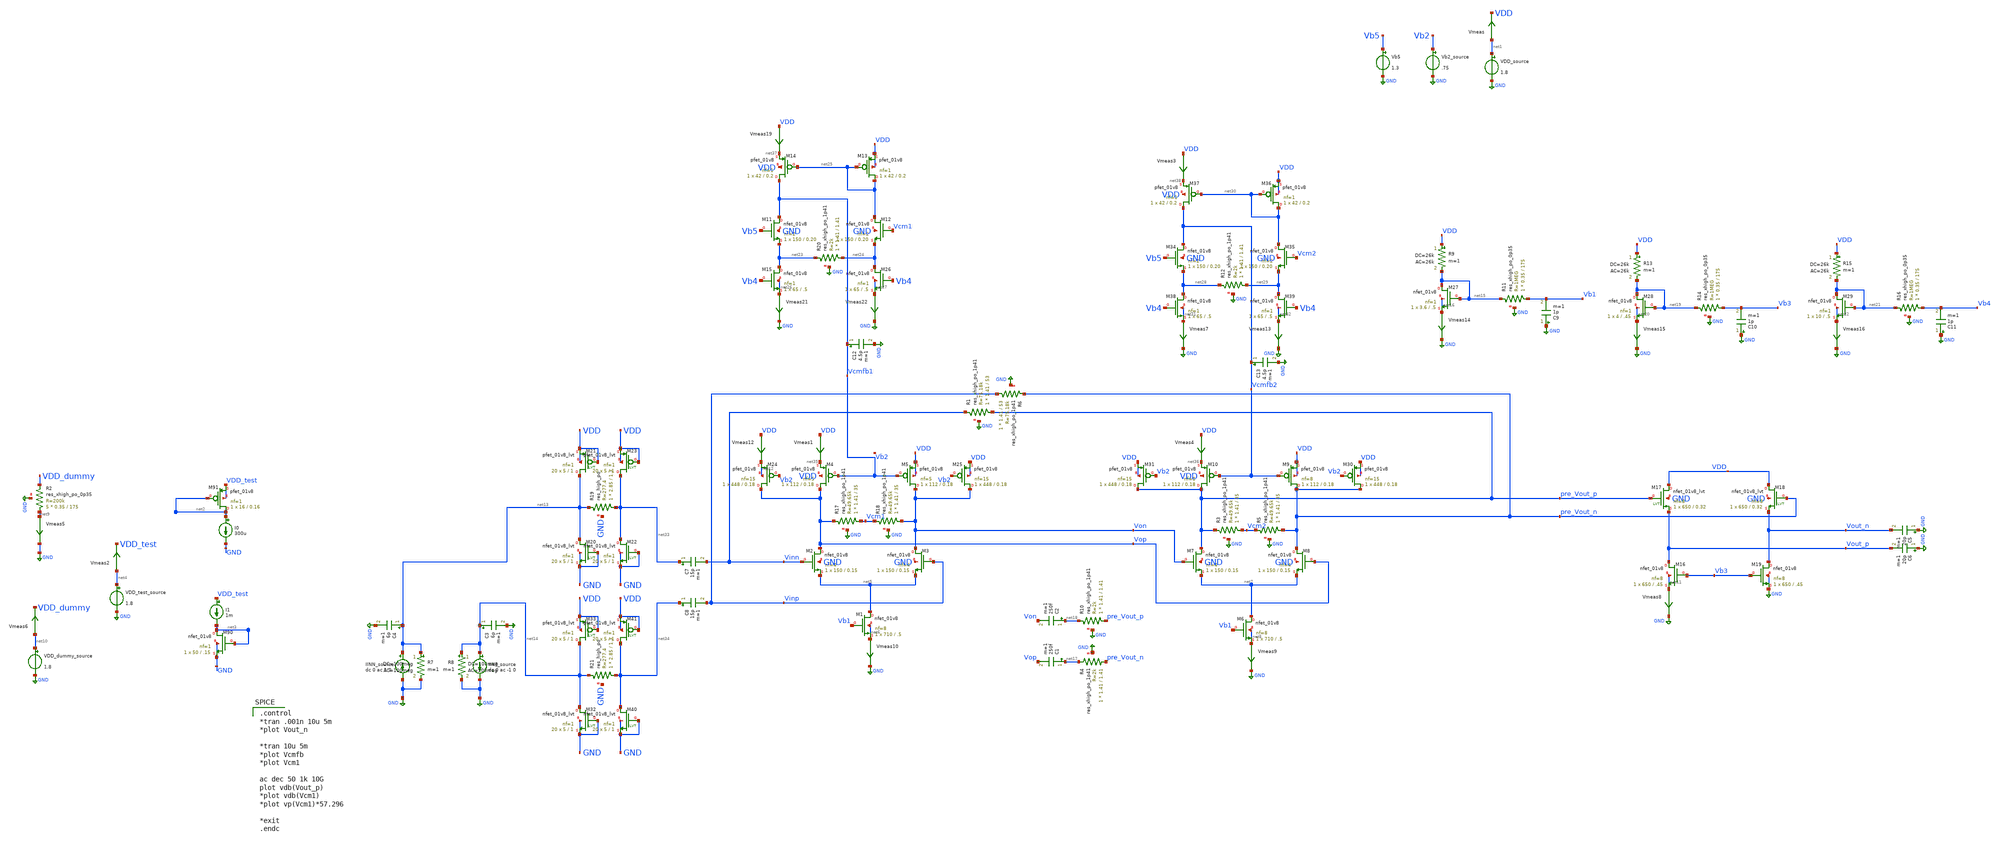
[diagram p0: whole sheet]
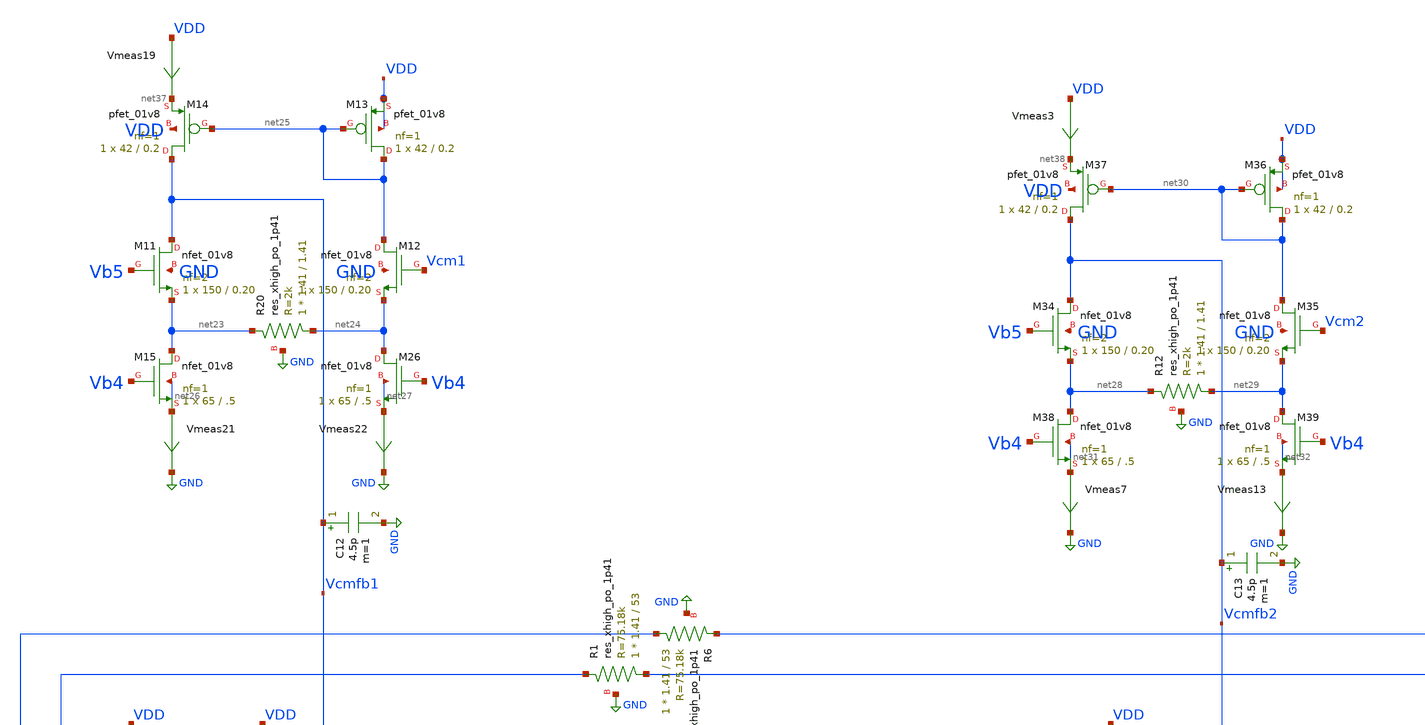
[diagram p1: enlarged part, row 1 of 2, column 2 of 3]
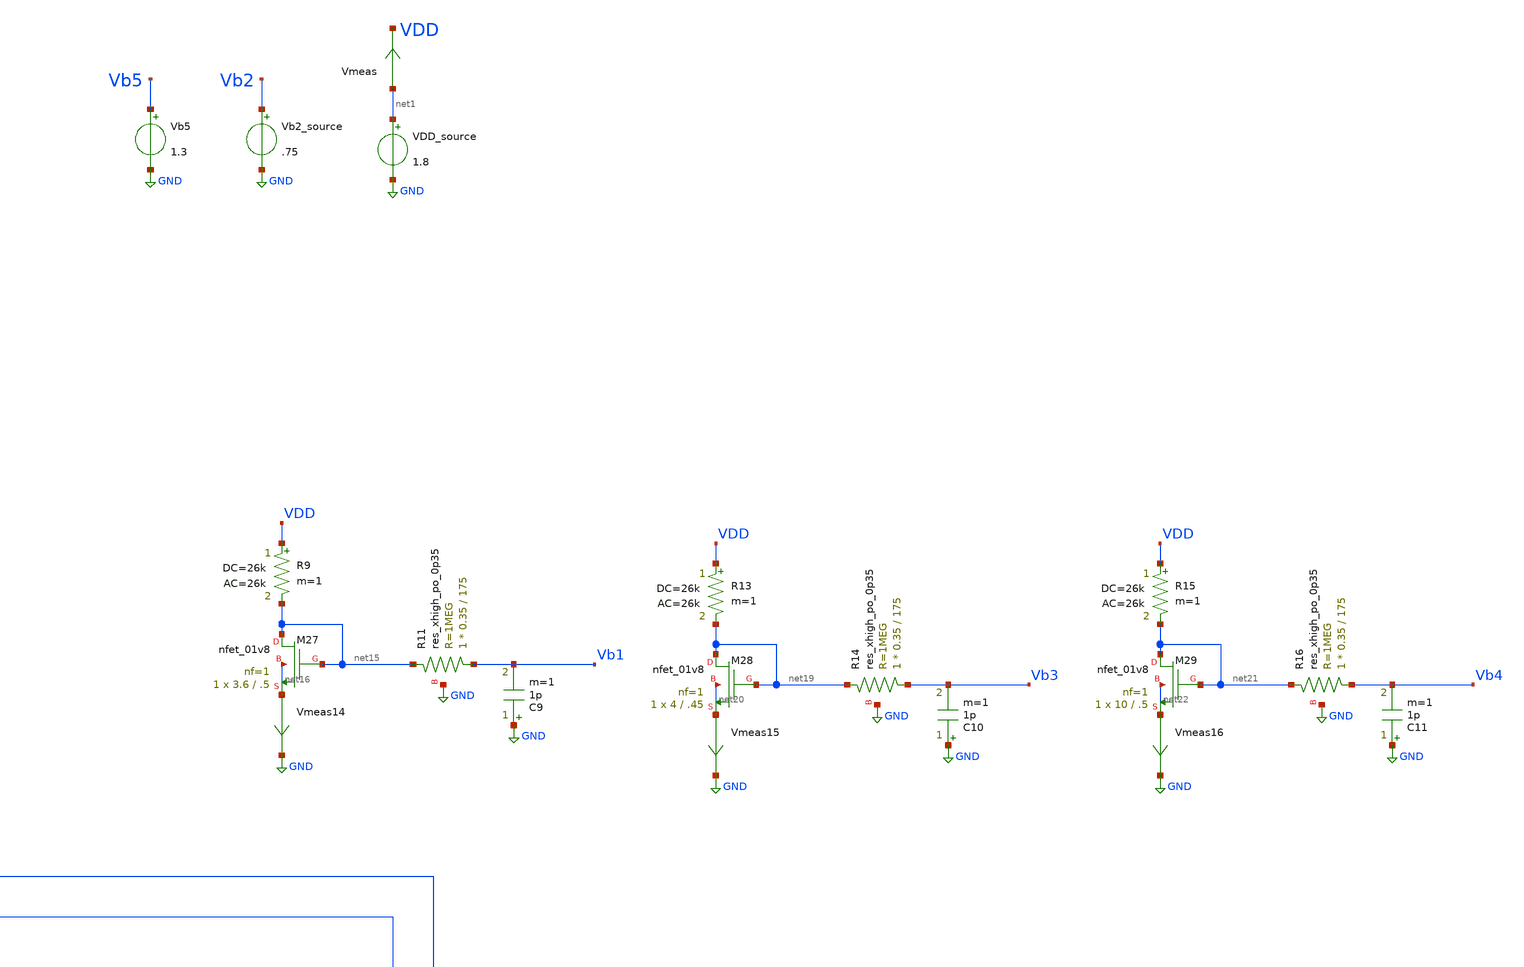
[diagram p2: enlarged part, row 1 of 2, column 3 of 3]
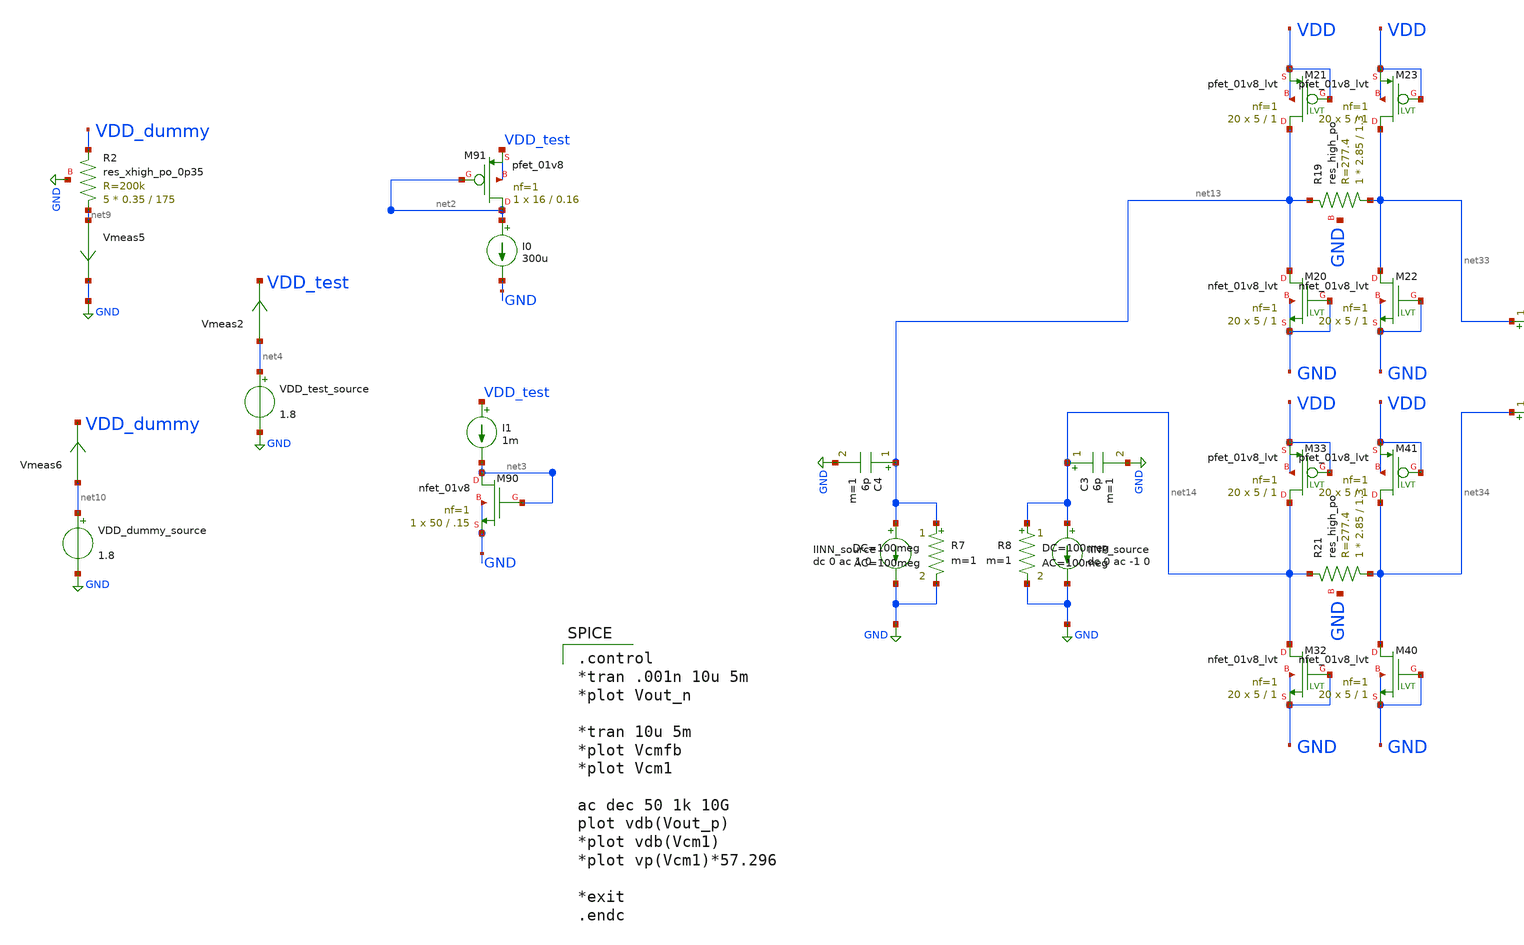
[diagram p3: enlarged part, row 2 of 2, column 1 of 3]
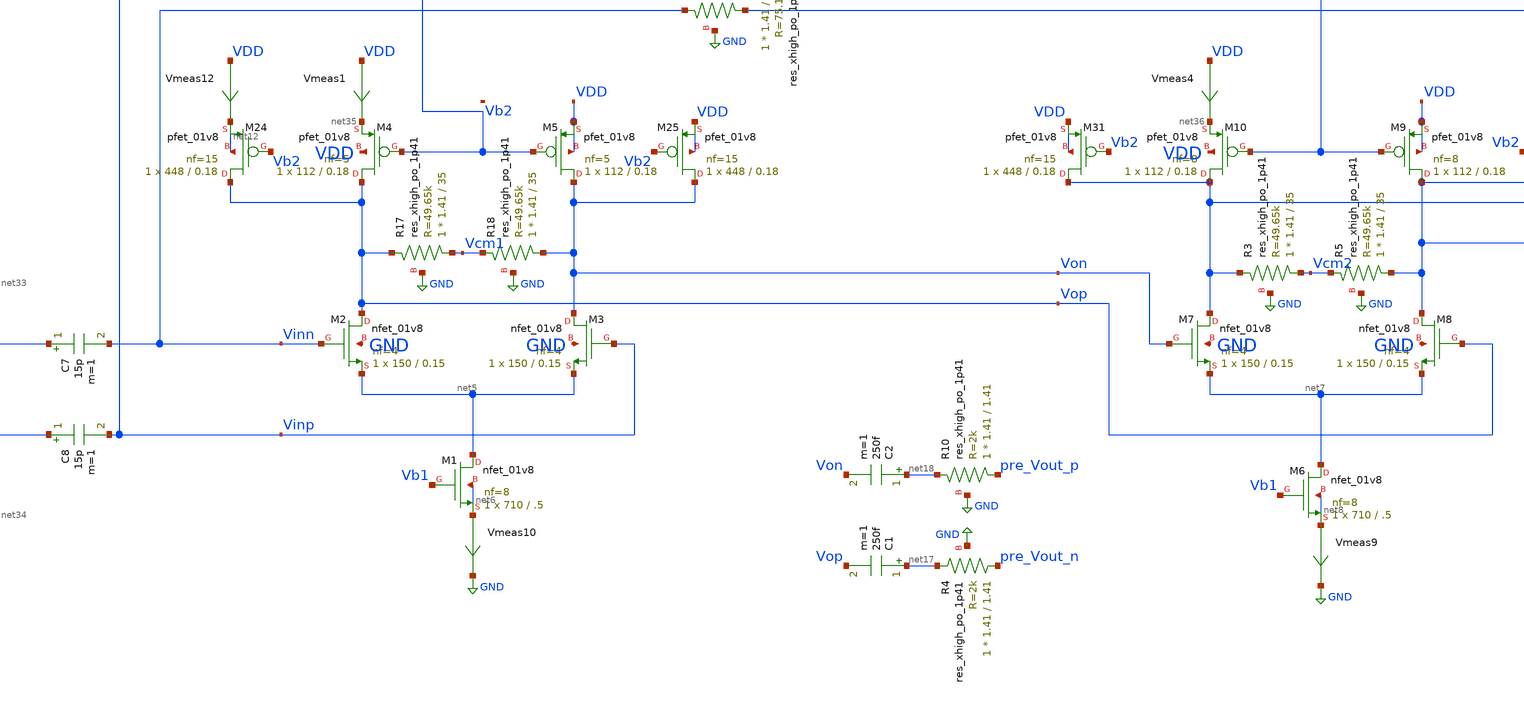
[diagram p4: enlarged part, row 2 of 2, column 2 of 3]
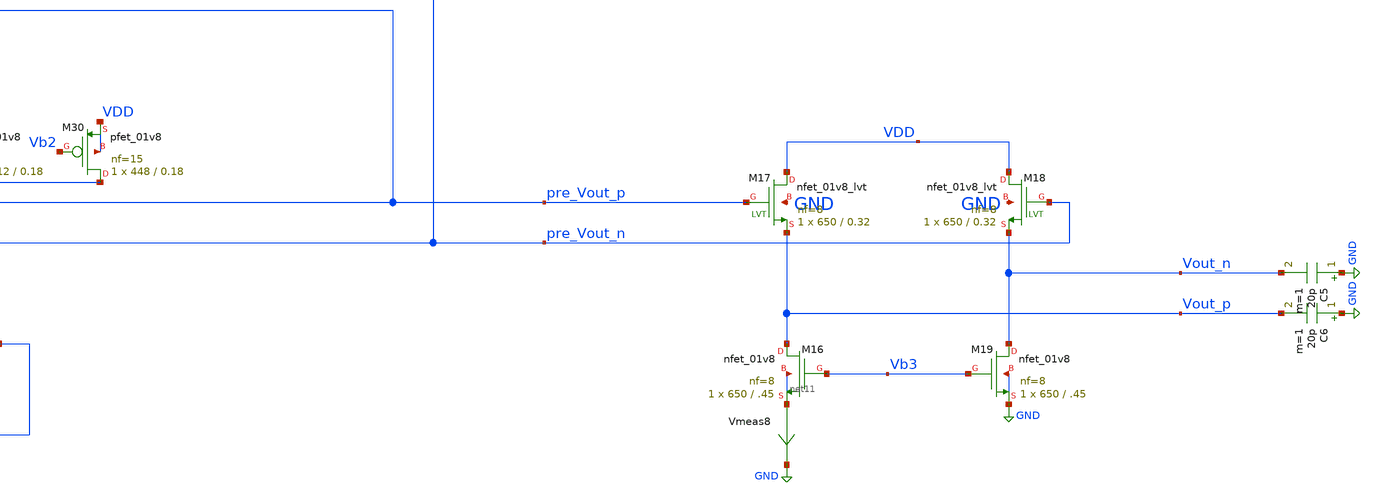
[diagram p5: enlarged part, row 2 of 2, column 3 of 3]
** sch_path: xschem/flattened_full_esd.sch
**.subckt flattened_full_esd
VDD_source net1 GND 1.8
Vmeas net1 VDD 0
.save i(vmeas)
XM90 net3 net3 GND GND sky130_fd_pr__nfet_01v8 L=.15 W=50 nf=1 ad='int((nf+1)/2) * W/nf * 0.29' as='int((nf+2)/2) * W/nf * 0.29'
+ pd='2*int((nf+1)/2) * (W/nf + 0.29)' ps='2*int((nf+2)/2) * (W/nf + 0.29)' nrd='0.29 / W' nrs='0.29 / W'
+ sa=0 sb=0 sd=0 mult=1 m=1
XM91 net2 net2 VDD_test VDD_test sky130_fd_pr__pfet_01v8 L=0.16 W=16 nf=1 ad='int((nf+1)/2) * W/nf * 0.29'
+ as='int((nf+2)/2) * W/nf * 0.29' pd='2*int((nf+1)/2) * (W/nf + 0.29)' ps='2*int((nf+2)/2) * (W/nf + 0.29)'
+ nrd='0.29 / W' nrs='0.29 / W' sa=0 sb=0 sd=0 mult=1 m=1
I0 net2 GND 300u
I1 VDD_test net3 1m
XM1 net5 Vb1 net6 net6 sky130_fd_pr__nfet_01v8 L=.5 W=710 nf=8 ad='int((nf+1)/2) * W/nf * 0.29' as='int((nf+2)/2) * W/nf * 0.29'
+ pd='2*int((nf+1)/2) * (W/nf + 0.29)' ps='2*int((nf+2)/2) * (W/nf + 0.29)' nrd='0.29 / W' nrs='0.29 / W'
+ sa=0 sb=0 sd=0 mult=1 m=1
VDD_test_source net4 GND 1.8
Vmeas2 net4 VDD_test 0
.save i(vmeas2)
XM2 Vop Vinn net5 GND sky130_fd_pr__nfet_01v8 L=0.15 W=150 nf=4 ad='int((nf+1)/2) * W/nf * 0.29' as='int((nf+2)/2) * W/nf * 0.29'
+ pd='2*int((nf+1)/2) * (W/nf + 0.29)' ps='2*int((nf+2)/2) * (W/nf + 0.29)' nrd='0.29 / W' nrs='0.29 / W'
+ sa=0 sb=0 sd=0 mult=1 m=1
XM3 Von Vinp net5 GND sky130_fd_pr__nfet_01v8 L=0.15 W=150 nf=4 ad='int((nf+1)/2) * W/nf * 0.29' as='int((nf+2)/2) * W/nf * 0.29'
+ pd='2*int((nf+1)/2) * (W/nf + 0.29)' ps='2*int((nf+2)/2) * (W/nf + 0.29)' nrd='0.29 / W' nrs='0.29 / W'
+ sa=0 sb=0 sd=0 mult=1 m=1
XM5 Von Vcmfb1 VDD VDD sky130_fd_pr__pfet_01v8 L=0.18 W=112 nf=5 ad='int((nf+1)/2) * W/nf * 0.29' as='int((nf+2)/2) * W/nf * 0.29'
+ pd='2*int((nf+1)/2) * (W/nf + 0.29)' ps='2*int((nf+2)/2) * (W/nf + 0.29)' nrd='0.29 / W' nrs='0.29 / W'
+ sa=0 sb=0 sd=0 mult=1 m=1
XM4 Vop Vcmfb1 net35 VDD sky130_fd_pr__pfet_01v8 L=0.18 W=112 nf=5 ad='int((nf+1)/2) * W/nf * 0.29' as='int((nf+2)/2) * W/nf * 0.29'
+ pd='2*int((nf+1)/2) * (W/nf + 0.29)' ps='2*int((nf+2)/2) * (W/nf + 0.29)' nrd='0.29 / W' nrs='0.29 / W'
+ sa=0 sb=0 sd=0 mult=1 m=1
Vb2_source Vb2 GND .75
Vmeas1 VDD net35 0
.save i(vmeas1)
XM6 net7 Vb1 net8 net8 sky130_fd_pr__nfet_01v8 L=.5 W=710 nf=8 ad='int((nf+1)/2) * W/nf * 0.29' as='int((nf+2)/2) * W/nf * 0.29'
+ pd='2*int((nf+1)/2) * (W/nf + 0.29)' ps='2*int((nf+2)/2) * (W/nf + 0.29)' nrd='0.29 / W' nrs='0.29 / W'
+ sa=0 sb=0 sd=0 mult=1 m=1
XM7 pre_Vout_p Von net7 GND sky130_fd_pr__nfet_01v8 L=0.15 W=150 nf=4 ad='int((nf+1)/2) * W/nf * 0.29'
+ as='int((nf+2)/2) * W/nf * 0.29' pd='2*int((nf+1)/2) * (W/nf + 0.29)' ps='2*int((nf+2)/2) * (W/nf + 0.29)'
+ nrd='0.29 / W' nrs='0.29 / W' sa=0 sb=0 sd=0 mult=1 m=1
XM8 pre_Vout_n Vop net7 GND sky130_fd_pr__nfet_01v8 L=0.15 W=150 nf=4 ad='int((nf+1)/2) * W/nf * 0.29'
+ as='int((nf+2)/2) * W/nf * 0.29' pd='2*int((nf+1)/2) * (W/nf + 0.29)' ps='2*int((nf+2)/2) * (W/nf + 0.29)'
+ nrd='0.29 / W' nrs='0.29 / W' sa=0 sb=0 sd=0 mult=1 m=1
XM9 pre_Vout_n Vcmfb2 VDD VDD sky130_fd_pr__pfet_01v8 L=0.18 W=112 nf=8 ad='int((nf+1)/2) * W/nf * 0.29'
+ as='int((nf+2)/2) * W/nf * 0.29' pd='2*int((nf+1)/2) * (W/nf + 0.29)' ps='2*int((nf+2)/2) * (W/nf + 0.29)'
+ nrd='0.29 / W' nrs='0.29 / W' sa=0 sb=0 sd=0 mult=1 m=1
XM10 pre_Vout_p Vcmfb2 net36 VDD sky130_fd_pr__pfet_01v8 L=0.18 W=112 nf=8 ad='int((nf+1)/2) * W/nf * 0.29'
+ as='int((nf+2)/2) * W/nf * 0.29' pd='2*int((nf+1)/2) * (W/nf + 0.29)' ps='2*int((nf+2)/2) * (W/nf + 0.29)'
+ nrd='0.29 / W' nrs='0.29 / W' sa=0 sb=0 sd=0 mult=1 m=1
Vmeas4 VDD net36 0
.save i(vmeas4)
Vmeas5 net9 GND 0
.save i(vmeas5)
C3 net14 GND 6p m=1
C4 net13 GND 6p m=1
VDD_dummy_source net10 GND 1.8
Vmeas6 net10 VDD_dummy 0
.save i(vmeas6)
IINN_source net13 GND dc 0 ac 1 0
IINP_source net14 GND dc 0 ac -1 0
XR6 Vinp pre_Vout_n GND sky130_fd_pr__res_xhigh_po_1p41 L=53 mult=1 m=1
XR1 pre_Vout_p Vinn GND sky130_fd_pr__res_xhigh_po_1p41 L=53 mult=1 m=1
XM16 Vout_p Vb3 net11 net11 sky130_fd_pr__nfet_01v8 L=.45 W=650 nf=8 ad='int((nf+1)/2) * W/nf * 0.29'
+ as='int((nf+2)/2) * W/nf * 0.29' pd='2*int((nf+1)/2) * (W/nf + 0.29)' ps='2*int((nf+2)/2) * (W/nf + 0.29)'
+ nrd='0.29 / W' nrs='0.29 / W' sa=0 sb=0 sd=0 mult=1 m=1
XM19 Vout_n Vb3 GND GND sky130_fd_pr__nfet_01v8 L=.45 W=650 nf=8 ad='int((nf+1)/2) * W/nf * 0.29' as='int((nf+2)/2) * W/nf * 0.29'
+ pd='2*int((nf+1)/2) * (W/nf + 0.29)' ps='2*int((nf+2)/2) * (W/nf + 0.29)' nrd='0.29 / W' nrs='0.29 / W'
+ sa=0 sb=0 sd=0 mult=1 m=1
Vmeas8 net11 GND 0
.save i(vmeas8)
XM17 VDD pre_Vout_p Vout_p GND sky130_fd_pr__nfet_01v8_lvt L=0.32 W=650 nf=8 ad='int((nf+1)/2) * W/nf * 0.29'
+ as='int((nf+2)/2) * W/nf * 0.29' pd='2*int((nf+1)/2) * (W/nf + 0.29)' ps='2*int((nf+2)/2) * (W/nf + 0.29)'
+ nrd='0.29 / W' nrs='0.29 / W' sa=0 sb=0 sd=0 mult=1 m=1
XM18 VDD pre_Vout_n Vout_n GND sky130_fd_pr__nfet_01v8_lvt L=0.32 W=650 nf=8 ad='int((nf+1)/2) * W/nf * 0.29'
+ as='int((nf+2)/2) * W/nf * 0.29' pd='2*int((nf+1)/2) * (W/nf + 0.29)' ps='2*int((nf+2)/2) * (W/nf + 0.29)'
+ nrd='0.29 / W' nrs='0.29 / W' sa=0 sb=0 sd=0 mult=1 m=1
C5 GND Vout_n 20p m=1
C6 GND Vout_p 20p m=1
Vmeas9 net8 GND 0
.save i(vmeas9)
Vmeas10 net6 GND 0
.save i(vmeas10)
XM24 Vop Vb2 net12 net12 sky130_fd_pr__pfet_01v8 L=0.18 W=448 nf=15 ad='int((nf+1)/2) * W/nf * 0.29'
+ as='int((nf+2)/2) * W/nf * 0.29' pd='2*int((nf+1)/2) * (W/nf + 0.29)' ps='2*int((nf+2)/2) * (W/nf + 0.29)'
+ nrd='0.29 / W' nrs='0.29 / W' sa=0 sb=0 sd=0 mult=1 m=1
XM25 Von Vb2 VDD VDD sky130_fd_pr__pfet_01v8 L=0.18 W=448 nf=15 ad='int((nf+1)/2) * W/nf * 0.29' as='int((nf+2)/2) * W/nf * 0.29'
+ pd='2*int((nf+1)/2) * (W/nf + 0.29)' ps='2*int((nf+2)/2) * (W/nf + 0.29)' nrd='0.29 / W' nrs='0.29 / W'
+ sa=0 sb=0 sd=0 mult=1 m=1
Vmeas12 VDD net12 0
.save i(vmeas12)
XM27 net15 net15 net16 net16 sky130_fd_pr__nfet_01v8 L=.5 W=3.6 nf=1 ad='int((nf+1)/2) * W/nf * 0.29'
+ as='int((nf+2)/2) * W/nf * 0.29' pd='2*int((nf+1)/2) * (W/nf + 0.29)' ps='2*int((nf+2)/2) * (W/nf + 0.29)'
+ nrd='0.29 / W' nrs='0.29 / W' sa=0 sb=0 sd=0 mult=1 m=1
Vmeas14 net16 GND 0
.save i(vmeas14)
R9 VDD net15 26k ac=26k m=1
R7 net13 GND 100meg ac=100meg m=1
R8 net14 GND 100meg ac=100meg m=1
C2 net18 Von 250f m=1
C1 net17 Vop 250f m=1
XR3 Vcm2 pre_Vout_p GND sky130_fd_pr__res_xhigh_po_1p41 L=35 mult=1 m=1
XR5 pre_Vout_n Vcm2 GND sky130_fd_pr__res_xhigh_po_1p41 L=35 mult=1 m=1
XR4 pre_Vout_n net17 GND sky130_fd_pr__res_xhigh_po_1p41 L=1.41 mult=1 m=1
XR10 pre_Vout_p net18 GND sky130_fd_pr__res_xhigh_po_1p41 L=1.41 mult=1 m=1
XR2 net9 VDD_dummy GND sky130_fd_pr__res_xhigh_po_0p35 L=175 mult=5 m=5
XR11 Vb1 net15 GND sky130_fd_pr__res_xhigh_po_0p35 L=175 mult=1 m=1
C9 GND Vb1 1p m=1
XM28 net19 net19 net20 net20 sky130_fd_pr__nfet_01v8 L=.45 W=4 nf=1 ad='int((nf+1)/2) * W/nf * 0.29'
+ as='int((nf+2)/2) * W/nf * 0.29' pd='2*int((nf+1)/2) * (W/nf + 0.29)' ps='2*int((nf+2)/2) * (W/nf + 0.29)'
+ nrd='0.29 / W' nrs='0.29 / W' sa=0 sb=0 sd=0 mult=1 m=1
Vmeas15 net20 GND 0
.save i(vmeas15)
R13 VDD net19 26k ac=26k m=1
XR14 Vb3 net19 GND sky130_fd_pr__res_xhigh_po_0p35 L=175 mult=1 m=1
C10 GND Vb3 1p m=1
XM29 net21 net21 net22 net22 sky130_fd_pr__nfet_01v8 L=.5 W=10 nf=1 ad='int((nf+1)/2) * W/nf * 0.29'
+ as='int((nf+2)/2) * W/nf * 0.29' pd='2*int((nf+1)/2) * (W/nf + 0.29)' ps='2*int((nf+2)/2) * (W/nf + 0.29)'
+ nrd='0.29 / W' nrs='0.29 / W' sa=0 sb=0 sd=0 mult=1 m=1
Vmeas16 net22 GND 0
.save i(vmeas16)
R15 VDD net21 26k ac=26k m=1
XR16 Vb4 net21 GND sky130_fd_pr__res_xhigh_po_0p35 L=175 mult=1 m=1
C11 GND Vb4 1p m=1
XR17 Vcm1 Vop GND sky130_fd_pr__res_xhigh_po_1p41 L=35 mult=1 m=1
XR18 Von Vcm1 GND sky130_fd_pr__res_xhigh_po_1p41 L=35 mult=1 m=1
XM30 pre_Vout_n Vb2 VDD VDD sky130_fd_pr__pfet_01v8 L=0.18 W=448 nf=15 ad='int((nf+1)/2) * W/nf * 0.29'
+ as='int((nf+2)/2) * W/nf * 0.29' pd='2*int((nf+1)/2) * (W/nf + 0.29)' ps='2*int((nf+2)/2) * (W/nf + 0.29)'
+ nrd='0.29 / W' nrs='0.29 / W' sa=0 sb=0 sd=0 mult=1 m=1
XM31 pre_Vout_p Vb2 VDD VDD sky130_fd_pr__pfet_01v8 L=0.18 W=448 nf=15 ad='int((nf+1)/2) * W/nf * 0.29'
+ as='int((nf+2)/2) * W/nf * 0.29' pd='2*int((nf+1)/2) * (W/nf + 0.29)' ps='2*int((nf+2)/2) * (W/nf + 0.29)'
+ nrd='0.29 / W' nrs='0.29 / W' sa=0 sb=0 sd=0 mult=1 m=1
XM11 Vcmfb1 Vb5 net23 GND sky130_fd_pr__nfet_01v8 L=0.20 W=150 nf=2 ad='int((nf+1)/2) * W/nf * 0.29'
+ as='int((nf+2)/2) * W/nf * 0.29' pd='2*int((nf+1)/2) * (W/nf + 0.29)' ps='2*int((nf+2)/2) * (W/nf + 0.29)'
+ nrd='0.29 / W' nrs='0.29 / W' sa=0 sb=0 sd=0 mult=1 m=1
XM12 net25 Vcm1 net24 GND sky130_fd_pr__nfet_01v8 L=0.20 W=150 nf=2 ad='int((nf+1)/2) * W/nf * 0.29'
+ as='int((nf+2)/2) * W/nf * 0.29' pd='2*int((nf+1)/2) * (W/nf + 0.29)' ps='2*int((nf+2)/2) * (W/nf + 0.29)'
+ nrd='0.29 / W' nrs='0.29 / W' sa=0 sb=0 sd=0 mult=1 m=1
XM13 net25 net25 VDD VDD sky130_fd_pr__pfet_01v8 L=0.2 W=42 nf=1 ad='int((nf+1)/2) * W/nf * 0.29' as='int((nf+2)/2) * W/nf * 0.29'
+ pd='2*int((nf+1)/2) * (W/nf + 0.29)' ps='2*int((nf+2)/2) * (W/nf + 0.29)' nrd='0.29 / W' nrs='0.29 / W'
+ sa=0 sb=0 sd=0 mult=1 m=1
XM14 Vcmfb1 net25 net37 VDD sky130_fd_pr__pfet_01v8 L=0.2 W=42 nf=1 ad='int((nf+1)/2) * W/nf * 0.29'
+ as='int((nf+2)/2) * W/nf * 0.29' pd='2*int((nf+1)/2) * (W/nf + 0.29)' ps='2*int((nf+2)/2) * (W/nf + 0.29)'
+ nrd='0.29 / W' nrs='0.29 / W' sa=0 sb=0 sd=0 mult=1 m=1
Vmeas19 VDD net37 0
.save i(vmeas19)
XM15 net23 Vb4 net26 net26 sky130_fd_pr__nfet_01v8 L=.5 W=65 nf=1 ad='int((nf+1)/2) * W/nf * 0.29' as='int((nf+2)/2) * W/nf * 0.29'
+ pd='2*int((nf+1)/2) * (W/nf + 0.29)' ps='2*int((nf+2)/2) * (W/nf + 0.29)' nrd='0.29 / W' nrs='0.29 / W'
+ sa=0 sb=0 sd=0 mult=1 m=1
Vmeas21 net26 GND 0
.save i(vmeas21)
XM26 net24 Vb4 net27 net27 sky130_fd_pr__nfet_01v8 L=.5 W=65 nf=1 ad='int((nf+1)/2) * W/nf * 0.29' as='int((nf+2)/2) * W/nf * 0.29'
+ pd='2*int((nf+1)/2) * (W/nf + 0.29)' ps='2*int((nf+2)/2) * (W/nf + 0.29)' nrd='0.29 / W' nrs='0.29 / W'
+ sa=0 sb=0 sd=0 mult=1 m=1
Vmeas22 net27 GND 0
.save i(vmeas22)
XR20 net24 net23 GND sky130_fd_pr__res_xhigh_po_1p41 L=1.41 mult=1 m=1
C7 net33 Vinn 15p m=1
C8 net34 Vinp 15p m=1
XM34 Vcmfb2 Vb5 net28 GND sky130_fd_pr__nfet_01v8 L=0.20 W=150 nf=2 ad='int((nf+1)/2) * W/nf * 0.29'
+ as='int((nf+2)/2) * W/nf * 0.29' pd='2*int((nf+1)/2) * (W/nf + 0.29)' ps='2*int((nf+2)/2) * (W/nf + 0.29)'
+ nrd='0.29 / W' nrs='0.29 / W' sa=0 sb=0 sd=0 mult=1 m=1
XM35 net30 Vcm2 net29 GND sky130_fd_pr__nfet_01v8 L=0.20 W=150 nf=2 ad='int((nf+1)/2) * W/nf * 0.29'
+ as='int((nf+2)/2) * W/nf * 0.29' pd='2*int((nf+1)/2) * (W/nf + 0.29)' ps='2*int((nf+2)/2) * (W/nf + 0.29)'
+ nrd='0.29 / W' nrs='0.29 / W' sa=0 sb=0 sd=0 mult=1 m=1
XM36 net30 net30 VDD VDD sky130_fd_pr__pfet_01v8 L=0.2 W=42 nf=1 ad='int((nf+1)/2) * W/nf * 0.29' as='int((nf+2)/2) * W/nf * 0.29'
+ pd='2*int((nf+1)/2) * (W/nf + 0.29)' ps='2*int((nf+2)/2) * (W/nf + 0.29)' nrd='0.29 / W' nrs='0.29 / W'
+ sa=0 sb=0 sd=0 mult=1 m=1
XM37 Vcmfb2 net30 net38 VDD sky130_fd_pr__pfet_01v8 L=0.2 W=42 nf=1 ad='int((nf+1)/2) * W/nf * 0.29'
+ as='int((nf+2)/2) * W/nf * 0.29' pd='2*int((nf+1)/2) * (W/nf + 0.29)' ps='2*int((nf+2)/2) * (W/nf + 0.29)'
+ nrd='0.29 / W' nrs='0.29 / W' sa=0 sb=0 sd=0 mult=1 m=1
Vmeas3 VDD net38 0
.save i(vmeas3)
XM38 net28 Vb4 net31 net31 sky130_fd_pr__nfet_01v8 L=.5 W=65 nf=1 ad='int((nf+1)/2) * W/nf * 0.29' as='int((nf+2)/2) * W/nf * 0.29'
+ pd='2*int((nf+1)/2) * (W/nf + 0.29)' ps='2*int((nf+2)/2) * (W/nf + 0.29)' nrd='0.29 / W' nrs='0.29 / W'
+ sa=0 sb=0 sd=0 mult=1 m=1
Vmeas7 net31 GND 0
.save i(vmeas7)
XM39 net29 Vb4 net32 net32 sky130_fd_pr__nfet_01v8 L=.5 W=65 nf=1 ad='int((nf+1)/2) * W/nf * 0.29' as='int((nf+2)/2) * W/nf * 0.29'
+ pd='2*int((nf+1)/2) * (W/nf + 0.29)' ps='2*int((nf+2)/2) * (W/nf + 0.29)' nrd='0.29 / W' nrs='0.29 / W'
+ sa=0 sb=0 sd=0 mult=1 m=1
Vmeas13 net32 GND 0
.save i(vmeas13)
XR12 net29 net28 GND sky130_fd_pr__res_xhigh_po_1p41 L=1.41 mult=1 m=1
Vb5 Vb5 GND 1.3
C12 Vcmfb1 GND 4.5p m=1
C13 Vcmfb2 GND 4.5p m=1
XM20 net13 GND GND GND sky130_fd_pr__nfet_01v8_lvt L=1 W=5 nf=1 ad='int((nf+1)/2) * W/nf * 0.29' as='int((nf+2)/2) * W/nf * 0.29'
+ pd='2*int((nf+1)/2) * (W/nf + 0.29)' ps='2*int((nf+2)/2) * (W/nf + 0.29)' nrd='0.29 / W' nrs='0.29 / W'
+ sa=0 sb=0 sd=0 mult=20 m=20
XM21 net13 VDD VDD VDD sky130_fd_pr__pfet_01v8_lvt L=1 W=5 nf=1 ad='int((nf+1)/2) * W/nf * 0.29' as='int((nf+2)/2) * W/nf * 0.29'
+ pd='2*int((nf+1)/2) * (W/nf + 0.29)' ps='2*int((nf+2)/2) * (W/nf + 0.29)' nrd='0.29 / W' nrs='0.29 / W'
+ sa=0 sb=0 sd=0 mult=20 m=20
XM22 net33 GND GND GND sky130_fd_pr__nfet_01v8_lvt L=1 W=5 nf=1 ad='int((nf+1)/2) * W/nf * 0.29' as='int((nf+2)/2) * W/nf * 0.29'
+ pd='2*int((nf+1)/2) * (W/nf + 0.29)' ps='2*int((nf+2)/2) * (W/nf + 0.29)' nrd='0.29 / W' nrs='0.29 / W'
+ sa=0 sb=0 sd=0 mult=20 m=20
XM23 net33 VDD VDD VDD sky130_fd_pr__pfet_01v8_lvt L=1 W=5 nf=1 ad='int((nf+1)/2) * W/nf * 0.29' as='int((nf+2)/2) * W/nf * 0.29'
+ pd='2*int((nf+1)/2) * (W/nf + 0.29)' ps='2*int((nf+2)/2) * (W/nf + 0.29)' nrd='0.29 / W' nrs='0.29 / W'
+ sa=0 sb=0 sd=0 mult=20 m=20
XR19 net33 net13 GND sky130_fd_pr__res_high_po W=2.85 L=1.3 mult=1 m=1
XM32 net14 GND GND GND sky130_fd_pr__nfet_01v8_lvt L=1 W=5 nf=1 ad='int((nf+1)/2) * W/nf * 0.29' as='int((nf+2)/2) * W/nf * 0.29'
+ pd='2*int((nf+1)/2) * (W/nf + 0.29)' ps='2*int((nf+2)/2) * (W/nf + 0.29)' nrd='0.29 / W' nrs='0.29 / W'
+ sa=0 sb=0 sd=0 mult=20 m=20
XM33 net14 VDD VDD VDD sky130_fd_pr__pfet_01v8_lvt L=1 W=5 nf=1 ad='int((nf+1)/2) * W/nf * 0.29' as='int((nf+2)/2) * W/nf * 0.29'
+ pd='2*int((nf+1)/2) * (W/nf + 0.29)' ps='2*int((nf+2)/2) * (W/nf + 0.29)' nrd='0.29 / W' nrs='0.29 / W'
+ sa=0 sb=0 sd=0 mult=20 m=20
XM40 net34 GND GND GND sky130_fd_pr__nfet_01v8_lvt L=1 W=5 nf=1 ad='int((nf+1)/2) * W/nf * 0.29' as='int((nf+2)/2) * W/nf * 0.29'
+ pd='2*int((nf+1)/2) * (W/nf + 0.29)' ps='2*int((nf+2)/2) * (W/nf + 0.29)' nrd='0.29 / W' nrs='0.29 / W'
+ sa=0 sb=0 sd=0 mult=20 m=20
XM41 net34 VDD VDD VDD sky130_fd_pr__pfet_01v8_lvt L=1 W=5 nf=1 ad='int((nf+1)/2) * W/nf * 0.29' as='int((nf+2)/2) * W/nf * 0.29'
+ pd='2*int((nf+1)/2) * (W/nf + 0.29)' ps='2*int((nf+2)/2) * (W/nf + 0.29)' nrd='0.29 / W' nrs='0.29 / W'
+ sa=0 sb=0 sd=0 mult=20 m=20
XR21 net34 net14 GND sky130_fd_pr__res_high_po W=2.85 L=1.3 mult=1 m=1
**** begin user architecture code

.include $::SKYWATER_MODELS/cells/nfet_01v8/sky130_fd_pr__nfet_01v8__tt.corner.spice
.include $::SKYWATER_MODELS/cells/pfet_01v8/sky130_fd_pr__pfet_01v8__tt.corner.spice
.include $::SKYWATER_MODELS/cells/nfet_01v8_lvt/sky130_fd_pr__nfet_01v8_lvt__tt.corner.spice
.include $::SKYWATER_MODELS/cells/pfet_01v8_lvt/sky130_fd_pr__pfet_01v8_lvt__tt.corner.spice
*.include $::SKYWATER_MODELS/cells/nfet_03v3_nvt/sky130_fd_pr__nfet_03v3_nvt__tt.corner.spice
*.include $::SKYWATER_MODELS/cells/nfet_05v0_nvt/sky130_fd_pr__nfet_05v0_nvt__tt.corner.spice
*.include $::SKYWATER_MODELS/cells/esd_nfet_01v8/sky130_fd_pr__esd_nfet_01v8__tt.corner.spice
*.include $::SKYWATER_MODELS/cells/pfet_01v8_hvt/sky130_fd_pr__pfet_01v8_hvt__tt.corner.spice
*.include $::SKYWATER_MODELS/models/corners/tt/nonfet.spice
* Mismatch parameters
.include $::SKYWATER_MODELS/cells/nfet_01v8/sky130_fd_pr__nfet_01v8__mismatch.corner.spice
.include $::SKYWATER_MODELS/cells/pfet_01v8/sky130_fd_pr__pfet_01v8__mismatch.corner.spice
.include $::SKYWATER_MODELS/cells/nfet_01v8_lvt/sky130_fd_pr__nfet_01v8_lvt__mismatch.corner.spice
.include $::SKYWATER_MODELS/cells/pfet_01v8_lvt/sky130_fd_pr__pfet_01v8_lvt__mismatch.corner.spice
*.include $::SKYWATER_MODELS/cells/pfet_01v8_hvt/sky130_fd_pr__pfet_01v8_hvt__mismatch.corner.spice
*.include $::SKYWATER_MODELS/cells/nfet_g5v0d10v5/sky130_fd_pr__nfet_g5v0d10v5__mismatch.corner.spice
*.include $::SKYWATER_MODELS/cells/pfet_g5v0d10v5/sky130_fd_pr__pfet_g5v0d10v5__mismatch.corner.spice
*.include $::SKYWATER_MODELS/cells/nfet_05v0_nvt/sky130_fd_pr__nfet_05v0_nvt__mismatch.corner.spice
*.include $::SKYWATER_MODELS/cells/nfet_03v3_nvt/sky130_fd_pr__nfet_03v3_nvt__mismatch.corner.spice
* Resistor$::SKYWATER_MODELS/Capacitor
.include $::SKYWATER_MODELS/models/r+c/res_typical__cap_typical.spice
.include $::SKYWATER_MODELS/models/r+c/res_typical__cap_typical__lin.spice
* Special cells
*.include $::SKYWATER_MODELS/models/corners/tt/specialized_cells.spice
* All models
.include $::SKYWATER_MODELS/models/all.spice
* Corner
*.include $::SKYWATER_MODELS/models/corners/tt/rf.spice


.option savecurrents
.control
save all
*NFET

save @m.xm90.msky130_fd_pr__nfet_01v8[vds] @m.xm90.msky130_fd_pr__nfet_01v8[gm]
+ @m.xm90.msky130_fd_pr__nfet_01v8[vth] @m.xm90.msky130_fd_pr__nfet_01v8[vgs] @m.xm90.msky130_fd_pr__nfet_01v8[id]
+ @m.xm90.msky130_fd_pr__nfet_01v8[gds] @m.xm90.msky130_fd_pr__nfet_01v8[cgg] @m.xm90.msky130_fd_pr__nfet_01v8[cgs]
+ @m.xm90.msky130_fd_pr__nfet_01v8[cgd] @m.xm90.msky130_fd_pr__nfet_01v8[cgb] @m.xm90.msky130_fd_pr__nfet_01v8[cdg]
+ @m.xm90.msky130_fd_pr__nfet_01v8[cds] @m.xm90.msky130_fd_pr__nfet_01v8[cdd] @m.xm90.msky130_fd_pr__nfet_01v8[cdb]
+ @m.xm90.msky130_fd_pr__nfet_01v8[csg] @m.xm90.msky130_fd_pr__nfet_01v8[css] @m.xm90.msky130_fd_pr__nfet_01v8[csd]
+ @m.xm90.msky130_fd_pr__nfet_01v8[csb] @m.xm90.msky130_fd_pr__nfet_01v8[cbg] @m.xm90.msky130_fd_pr__nfet_01v8[cbs]
+ @m.xm90.msky130_fd_pr__nfet_01v8[cbd] @m.xm90.msky130_fd_pr__nfet_01v8[cbb]
save @m.xm1.msky130_fd_pr__nfet_01v8[vds] @m.xm1.msky130_fd_pr__nfet_01v8[gm]
+ @m.xm1.msky130_fd_pr__nfet_01v8[vth] @m.xm1.msky130_fd_pr__nfet_01v8[vgs] @m.xm1.msky130_fd_pr__nfet_01v8[id]
+ @m.xm1.msky130_fd_pr__nfet_01v8[gds] @m.xm1.msky130_fd_pr__nfet_01v8[cgg] @m.xm1.msky130_fd_pr__nfet_01v8[cgs]
+ @m.xm1.msky130_fd_pr__nfet_01v8[cgd] @m.xm1.msky130_fd_pr__nfet_01v8[cgb] @m.xm1.msky130_fd_pr__nfet_01v8[cdg]
+ @m.xm1.msky130_fd_pr__nfet_01v8[cds] @m.xm1.msky130_fd_pr__nfet_01v8[cdd] @m.xm1.msky130_fd_pr__nfet_01v8[cdb]
+ @m.xm1.msky130_fd_pr__nfet_01v8[csg] @m.xm1.msky130_fd_pr__nfet_01v8[css] @m.xm1.msky130_fd_pr__nfet_01v8[csd]
+ @m.xm1.msky130_fd_pr__nfet_01v8[csb] @m.xm1.msky130_fd_pr__nfet_01v8[cbg] @m.xm1.msky130_fd_pr__nfet_01v8[cbs]
+ @m.xm1.msky130_fd_pr__nfet_01v8[cbd] @m.xm1.msky130_fd_pr__nfet_01v8[cbb]
save @m.xm2.msky130_fd_pr__nfet_01v8[vds] @m.xm2.msky130_fd_pr__nfet_01v8[gm]
+ @m.xm2.msky130_fd_pr__nfet_01v8[vth] @m.xm2.msky130_fd_pr__nfet_01v8[vgs] @m.xm2.msky130_fd_pr__nfet_01v8[id]
+ @m.xm2.msky130_fd_pr__nfet_01v8[gds] @m.xm2.msky130_fd_pr__nfet_01v8[cgg] @m.xm2.msky130_fd_pr__nfet_01v8[cgs]
+ @m.xm2.msky130_fd_pr__nfet_01v8[cgd] @m.xm2.msky130_fd_pr__nfet_01v8[cgb] @m.xm2.msky130_fd_pr__nfet_01v8[cdg]
+ @m.xm2.msky130_fd_pr__nfet_01v8[cds] @m.xm2.msky130_fd_pr__nfet_01v8[cdd] @m.xm2.msky130_fd_pr__nfet_01v8[cdb]
+ @m.xm2.msky130_fd_pr__nfet_01v8[csg] @m.xm2.msky130_fd_pr__nfet_01v8[css] @m.xm2.msky130_fd_pr__nfet_01v8[csd]
+ @m.xm2.msky130_fd_pr__nfet_01v8[csb] @m.xm2.msky130_fd_pr__nfet_01v8[cbg] @m.xm2.msky130_fd_pr__nfet_01v8[cbs]
+ @m.xm2.msky130_fd_pr__nfet_01v8[cbd] @m.xm2.msky130_fd_pr__nfet_01v8[cbb]
save @m.xm3.msky130_fd_pr__nfet_01v8[vds] @m.xm3.msky130_fd_pr__nfet_01v8[gm]
+ @m.xm3.msky130_fd_pr__nfet_01v8[vth] @m.xm3.msky130_fd_pr__nfet_01v8[vgs] @m.xm3.msky130_fd_pr__nfet_01v8[id]
+ @m.xm3.msky130_fd_pr__nfet_01v8[gds] @m.xm3.msky130_fd_pr__nfet_01v8[cgg] @m.xm3.msky130_fd_pr__nfet_01v8[cgs]
+ @m.xm3.msky130_fd_pr__nfet_01v8[cgd] @m.xm3.msky130_fd_pr__nfet_01v8[cgb] @m.xm3.msky130_fd_pr__nfet_01v8[cdg]
+ @m.xm3.msky130_fd_pr__nfet_01v8[cds] @m.xm3.msky130_fd_pr__nfet_01v8[cdd] @m.xm3.msky130_fd_pr__nfet_01v8[cdb]
+ @m.xm3.msky130_fd_pr__nfet_01v8[csg] @m.xm3.msky130_fd_pr__nfet_01v8[css] @m.xm3.msky130_fd_pr__nfet_01v8[csd]
+ @m.xm3.msky130_fd_pr__nfet_01v8[csb] @m.xm3.msky130_fd_pr__nfet_01v8[cbg] @m.xm3.msky130_fd_pr__nfet_01v8[cbs]
+ @m.xm3.msky130_fd_pr__nfet_01v8[cbd] @m.xm3.msky130_fd_pr__nfet_01v8[cbb]
save @m.xm6.msky130_fd_pr__nfet_01v8[vds] @m.xm6.msky130_fd_pr__nfet_01v8[gm]
+ @m.xm6.msky130_fd_pr__nfet_01v8[vth] @m.xm6.msky130_fd_pr__nfet_01v8[vgs] @m.xm6.msky130_fd_pr__nfet_01v8[id]
+ @m.xm6.msky130_fd_pr__nfet_01v8[gds] @m.xm6.msky130_fd_pr__nfet_01v8[cgg] @m.xm6.msky130_fd_pr__nfet_01v8[cgs]
+ @m.xm6.msky130_fd_pr__nfet_01v8[cgd] @m.xm6.msky130_fd_pr__nfet_01v8[cgb] @m.xm6.msky130_fd_pr__nfet_01v8[cdg]
+ @m.xm6.msky130_fd_pr__nfet_01v8[cds] @m.xm6.msky130_fd_pr__nfet_01v8[cdd] @m.xm6.msky130_fd_pr__nfet_01v8[cdb]
+ @m.xm6.msky130_fd_pr__nfet_01v8[csg] @m.xm6.msky130_fd_pr__nfet_01v8[css] @m.xm6.msky130_fd_pr__nfet_01v8[csd]
+ @m.xm6.msky130_fd_pr__nfet_01v8[csb] @m.xm6.msky130_fd_pr__nfet_01v8[cbg] @m.xm6.msky130_fd_pr__nfet_01v8[cbs]
+ @m.xm6.msky130_fd_pr__nfet_01v8[cbd] @m.xm6.msky130_fd_pr__nfet_01v8[cbb]
save @m.xm7.msky130_fd_pr__nfet_01v8[vds] @m.xm7.msky130_fd_pr__nfet_01v8[gm]
+ @m.xm7.msky130_fd_pr__nfet_01v8[vth] @m.xm7.msky130_fd_pr__nfet_01v8[vgs] @m.xm7.msky130_fd_pr__nfet_01v8[id]
+ @m.xm7.msky130_fd_pr__nfet_01v8[gds] @m.xm7.msky130_fd_pr__nfet_01v8[cgg] @m.xm7.msky130_fd_pr__nfet_01v8[cgs]
+ @m.xm7.msky130_fd_pr__nfet_01v8[cgd] @m.xm7.msky130_fd_pr__nfet_01v8[cgb] @m.xm7.msky130_fd_pr__nfet_01v8[cdg]
+ @m.xm7.msky130_fd_pr__nfet_01v8[cds] @m.xm7.msky130_fd_pr__nfet_01v8[cdd] @m.xm7.msky130_fd_pr__nfet_01v8[cdb]
+ @m.xm7.msky130_fd_pr__nfet_01v8[csg] @m.xm7.msky130_fd_pr__nfet_01v8[css] @m.xm7.msky130_fd_pr__nfet_01v8[csd]
+ @m.xm7.msky130_fd_pr__nfet_01v8[csb] @m.xm7.msky130_fd_pr__nfet_01v8[cbg] @m.xm7.msky130_fd_pr__nfet_01v8[cbs]
+ @m.xm7.msky130_fd_pr__nfet_01v8[cbd] @m.xm7.msky130_fd_pr__nfet_01v8[cbb]
save @m.xm8.msky130_fd_pr__nfet_01v8[vds] @m.xm8.msky130_fd_pr__nfet_01v8[gm]
+ @m.xm8.msky130_fd_pr__nfet_01v8[vth] @m.xm8.msky130_fd_pr__nfet_01v8[vgs] @m.xm8.msky130_fd_pr__nfet_01v8[id]
+ @m.xm8.msky130_fd_pr__nfet_01v8[gds] @m.xm8.msky130_fd_pr__nfet_01v8[cgg] @m.xm8.msky130_fd_pr__nfet_01v8[cgs]
+ @m.xm8.msky130_fd_pr__nfet_01v8[cgd] @m.xm8.msky130_fd_pr__nfet_01v8[cgb] @m.xm8.msky130_fd_pr__nfet_01v8[cdg]
+ @m.xm8.msky130_fd_pr__nfet_01v8[cds] @m.xm8.msky130_fd_pr__nfet_01v8[cdd] @m.xm8.msky130_fd_pr__nfet_01v8[cdb]
+ @m.xm8.msky130_fd_pr__nfet_01v8[csg] @m.xm8.msky130_fd_pr__nfet_01v8[css] @m.xm8.msky130_fd_pr__nfet_01v8[csd]
+ @m.xm8.msky130_fd_pr__nfet_01v8[csb] @m.xm8.msky130_fd_pr__nfet_01v8[cbg] @m.xm8.msky130_fd_pr__nfet_01v8[cbs]
+ @m.xm8.msky130_fd_pr__nfet_01v8[cbd] @m.xm8.msky130_fd_pr__nfet_01v8[cbb]
save @m.xm11.msky130_fd_pr__nfet_01v8[vds] @m.xm11.msky130_fd_pr__nfet_01v8[gm]
+ @m.xm11.msky130_fd_pr__nfet_01v8[vth] @m.xm11.msky130_fd_pr__nfet_01v8[vgs] @m.xm11.msky130_fd_pr__nfet_01v8[id]
+ @m.xm11.msky130_fd_pr__nfet_01v8[gds] @m.xm11.msky130_fd_pr__nfet_01v8[cgg] @m.xm11.msky130_fd_pr__nfet_01v8[cgs]
+ @m.xm11.msky130_fd_pr__nfet_01v8[cgd] @m.xm11.msky130_fd_pr__nfet_01v8[cgb] @m.xm11.msky130_fd_pr__nfet_01v8[cdg]
+ @m.xm11.msky130_fd_pr__nfet_01v8[cds] @m.xm11.msky130_fd_pr__nfet_01v8[cdd] @m.xm11.msky130_fd_pr__nfet_01v8[cdb]
+ @m.xm11.msky130_fd_pr__nfet_01v8[csg] @m.xm11.msky130_fd_pr__nfet_01v8[css] @m.xm11.msky130_fd_pr__nfet_01v8[csd]
+ @m.xm11.msky130_fd_pr__nfet_01v8[csb] @m.xm11.msky130_fd_pr__nfet_01v8[cbg] @m.xm11.msky130_fd_pr__nfet_01v8[cbs]
+ @m.xm11.msky130_fd_pr__nfet_01v8[cbd] @m.xm11.msky130_fd_pr__nfet_01v8[cbb]
save @m.xm12.msky130_fd_pr__nfet_01v8[vds] @m.xm12.msky130_fd_pr__nfet_01v8[gm]
+ @m.xm12.msky130_fd_pr__nfet_01v8[vth] @m.xm12.msky130_fd_pr__nfet_01v8[vgs] @m.xm12.msky130_fd_pr__nfet_01v8[id]
+ @m.xm12.msky130_fd_pr__nfet_01v8[gds] @m.xm12.msky130_fd_pr__nfet_01v8[cgg] @m.xm12.msky130_fd_pr__nfet_01v8[cgs]
+ @m.xm12.msky130_fd_pr__nfet_01v8[cgd] @m.xm12.msky130_fd_pr__nfet_01v8[cgb] @m.xm12.msky130_fd_pr__nfet_01v8[cdg]
+ @m.xm12.msky130_fd_pr__nfet_01v8[cds] @m.xm12.msky130_fd_pr__nfet_01v8[cdd] @m.xm12.msky130_fd_pr__nfet_01v8[cdb]
+ @m.xm12.msky130_fd_pr__nfet_01v8[csg] @m.xm12.msky130_fd_pr__nfet_01v8[css] @m.xm12.msky130_fd_pr__nfet_01v8[csd]
+ @m.xm12.msky130_fd_pr__nfet_01v8[csb] @m.xm12.msky130_fd_pr__nfet_01v8[cbg] @m.xm12.msky130_fd_pr__nfet_01v8[cbs]
+ @m.xm12.msky130_fd_pr__nfet_01v8[cbd] @m.xm12.msky130_fd_pr__nfet_01v8[cbb]
save @m.xm16.msky130_fd_pr__nfet_01v8[vds] @m.xm16.msky130_fd_pr__nfet_01v8[gm]
+ @m.xm16.msky130_fd_pr__nfet_01v8[vth] @m.xm16.msky130_fd_pr__nfet_01v8[vgs] @m.xm16.msky130_fd_pr__nfet_01v8[id]
+ @m.xm16.msky130_fd_pr__nfet_01v8[gds] @m.xm16.msky130_fd_pr__nfet_01v8[cgg] @m.xm16.msky130_fd_pr__nfet_01v8[cgs]
+ @m.xm16.msky130_fd_pr__nfet_01v8[cgd] @m.xm16.msky130_fd_pr__nfet_01v8[cgb] @m.xm16.msky130_fd_pr__nfet_01v8[cdg]
+ @m.xm16.msky130_fd_pr__nfet_01v8[cds] @m.xm16.msky130_fd_pr__nfet_01v8[cdd] @m.xm16.msky130_fd_pr__nfet_01v8[cdb]
+ @m.xm16.msky130_fd_pr__nfet_01v8[csg] @m.xm16.msky130_fd_pr__nfet_01v8[css] @m.xm16.msky130_fd_pr__nfet_01v8[csd]
+ @m.xm16.msky130_fd_pr__nfet_01v8[csb] @m.xm16.msky130_fd_pr__nfet_01v8[cbg] @m.xm16.msky130_fd_pr__nfet_01v8[cbs]
+ @m.xm16.msky130_fd_pr__nfet_01v8[cbd] @m.xm16.msky130_fd_pr__nfet_01v8[cbb]
save @m.xm17.msky130_fd_pr__nfet_01v8_lvt[vds] @m.xm17.msky130_fd_pr__nfet_01v8_lvt[gm]
+ @m.xm17.msky130_fd_pr__nfet_01v8_lvt[vth] @m.xm17.msky130_fd_pr__nfet_01v8_lvt[vgs] @m.xm17.msky130_fd_pr__nfet_01v8_lvt[id]
+ @m.xm17.msky130_fd_pr__nfet_01v8_lvt[gds] @m.xm17.msky130_fd_pr__nfet_01v8_lvt[cgg] @m.xm17.msky130_fd_pr__nfet_01v8_lvt[cgs]
+ @m.xm17.msky130_fd_pr__nfet_01v8_lvt[cgd] @m.xm17.msky130_fd_pr__nfet_01v8_lvt[cgb] @m.xm17.msky130_fd_pr__nfet_01v8_lvt[cdg]
+ @m.xm17.msky130_fd_pr__nfet_01v8_lvt[cds] @m.xm17.msky130_fd_pr__nfet_01v8_lvt[cdd] @m.xm17.msky130_fd_pr__nfet_01v8_lvt[cdb]
+ @m.xm17.msky130_fd_pr__nfet_01v8_lvt[csg] @m.xm17.msky130_fd_pr__nfet_01v8_lvt[css] @m.xm17.msky130_fd_pr__nfet_01v8_lvt[csd]
+ @m.xm17.msky130_fd_pr__nfet_01v8_lvt[csb] @m.xm17.msky130_fd_pr__nfet_01v8_lvt[cbg] @m.xm17.msky130_fd_pr__nfet_01v8_lvt[cbs]
+ @m.xm17.msky130_fd_pr__nfet_01v8_lvt[cbd] @m.xm17.msky130_fd_pr__nfet_01v8_lvt[cbb]
save @m.xm18.msky130_fd_pr__nfet_01v8_lvt[vds] @m.xm18.msky130_fd_pr__nfet_01v8_lvt[gm]
+ @m.xm18.msky130_fd_pr__nfet_01v8_lvt[vth] @m.xm18.msky130_fd_pr__nfet_01v8_lvt[vgs] @m.xm18.msky130_fd_pr__nfet_01v8_lvt[id]
+ @m.xm18.msky130_fd_pr__nfet_01v8_lvt[gds] @m.xm18.msky130_fd_pr__nfet_01v8_lvt[cgg] @m.xm18.msky130_fd_pr__nfet_01v8_lvt[cgs]
+ @m.xm18.msky130_fd_pr__nfet_01v8_lvt[cgd] @m.xm18.msky130_fd_pr__nfet_01v8_lvt[cgb] @m.xm18.msky130_fd_pr__nfet_01v8_lvt[cdg]
+ @m.xm18.msky130_fd_pr__nfet_01v8_lvt[cds] @m.xm18.msky130_fd_pr__nfet_01v8_lvt[cdd] @m.xm18.msky130_fd_pr__nfet_01v8_lvt[cdb]
+ @m.xm18.msky130_fd_pr__nfet_01v8_lvt[csg] @m.xm18.msky130_fd_pr__nfet_01v8_lvt[css] @m.xm18.msky130_fd_pr__nfet_01v8_lvt[csd]
+ @m.xm18.msky130_fd_pr__nfet_01v8_lvt[csb] @m.xm18.msky130_fd_pr__nfet_01v8_lvt[cbg] @m.xm18.msky130_fd_pr__nfet_01v8_lvt[cbs]
+ @m.xm18.msky130_fd_pr__nfet_01v8_lvt[cbd] @m.xm18.msky130_fd_pr__nfet_01v8_lvt[cbb]
save @m.xm19.msky130_fd_pr__nfet_01v8[vds] @m.xm19.msky130_fd_pr__nfet_01v8[gm]
+ @m.xm19.msky130_fd_pr__nfet_01v8[vth] @m.xm19.msky130_fd_pr__nfet_01v8[vgs] @m.xm19.msky130_fd_pr__nfet_01v8[id]
+ @m.xm19.msky130_fd_pr__nfet_01v8[gds] @m.xm19.msky130_fd_pr__nfet_01v8[cgg] @m.xm19.msky130_fd_pr__nfet_01v8[cgs]
+ @m.xm19.msky130_fd_pr__nfet_01v8[cgd] @m.xm19.msky130_fd_pr__nfet_01v8[cgb] @m.xm19.msky130_fd_pr__nfet_01v8[cdg]
+ @m.xm19.msky130_fd_pr__nfet_01v8[cds] @m.xm19.msky130_fd_pr__nfet_01v8[cdd] @m.xm19.msky130_fd_pr__nfet_01v8[cdb]
+ @m.xm19.msky130_fd_pr__nfet_01v8[csg] @m.xm19.msky130_fd_pr__nfet_01v8[css] @m.xm19.msky130_fd_pr__nfet_01v8[csd]
+ @m.xm19.msky130_fd_pr__nfet_01v8[csb] @m.xm19.msky130_fd_pr__nfet_01v8[cbg] @m.xm19.msky130_fd_pr__nfet_01v8[cbs]
+ @m.xm19.msky130_fd_pr__nfet_01v8[cbd] @m.xm19.msky130_fd_pr__nfet_01v8[cbb]
save @m.xm30.msky130_fd_pr__nfet_01v8[vds] @m.xm30.msky130_fd_pr__nfet_01v8[gm]
+ @m.xm30.msky130_fd_pr__nfet_01v8[vth] @m.xm30.msky130_fd_pr__nfet_01v8[vgs] @m.xm30.msky130_fd_pr__nfet_01v8[id]
+ @m.xm30.msky130_fd_pr__nfet_01v8[gds] @m.xm30.msky130_fd_pr__nfet_01v8[cgg] @m.xm30.msky130_fd_pr__nfet_01v8[cgs]
+ @m.xm30.msky130_fd_pr__nfet_01v8[cgd] @m.xm30.msky130_fd_pr__nfet_01v8[cgb] @m.xm30.msky130_fd_pr__nfet_01v8[cdg]
+ @m.xm30.msky130_fd_pr__nfet_01v8[cds] @m.xm30.msky130_fd_pr__nfet_01v8[cdd] @m.xm30.msky130_fd_pr__nfet_01v8[cdb]
+ @m.xm30.msky130_fd_pr__nfet_01v8[csg] @m.xm30.msky130_fd_pr__nfet_01v8[css] @m.xm30.msky130_fd_pr__nfet_01v8[csd]
+ @m.xm30.msky130_fd_pr__nfet_01v8[csb] @m.xm30.msky130_fd_pr__nfet_01v8[cbg] @m.xm30.msky130_fd_pr__nfet_01v8[cbs]
+ @m.xm30.msky130_fd_pr__nfet_01v8[cbd] @m.xm30.msky130_fd_pr__nfet_01v8[cbb]
save @m.xm26.msky130_fd_pr__nfet_01v8[vds] @m.xm26.msky130_fd_pr__nfet_01v8[gm]
+ @m.xm26.msky130_fd_pr__nfet_01v8[vth] @m.xm26.msky130_fd_pr__nfet_01v8[vgs] @m.xm26.msky130_fd_pr__nfet_01v8[id]
+ @m.xm26.msky130_fd_pr__nfet_01v8[gds] @m.xm26.msky130_fd_pr__nfet_01v8[cgg] @m.xm26.msky130_fd_pr__nfet_01v8[cgs]
+ @m.xm26.msky130_fd_pr__nfet_01v8[cgd] @m.xm26.msky130_fd_pr__nfet_01v8[cgb] @m.xm26.msky130_fd_pr__nfet_01v8[cdg]
+ @m.xm26.msky130_fd_pr__nfet_01v8[cds] @m.xm26.msky130_fd_pr__nfet_01v8[cdd] @m.xm26.msky130_fd_pr__nfet_01v8[cdb]
+ @m.xm26.msky130_fd_pr__nfet_01v8[csg] @m.xm26.msky130_fd_pr__nfet_01v8[css] @m.xm26.msky130_fd_pr__nfet_01v8[csd]
+ @m.xm26.msky130_fd_pr__nfet_01v8[csb] @m.xm26.msky130_fd_pr__nfet_01v8[cbg] @m.xm26.msky130_fd_pr__nfet_01v8[cbs]
+ @m.xm26.msky130_fd_pr__nfet_01v8[cbd] @m.xm26.msky130_fd_pr__nfet_01v8[cbb]
save @m.xm27.msky130_fd_pr__nfet_01v8[vds] @m.xm27.msky130_fd_pr__nfet_01v8[gm]
+ @m.xm27.msky130_fd_pr__nfet_01v8[vth] @m.xm27.msky130_fd_pr__nfet_01v8[vgs] @m.xm27.msky130_fd_pr__nfet_01v8[id]
+ @m.xm27.msky130_fd_pr__nfet_01v8[gds] @m.xm27.msky130_fd_pr__nfet_01v8[cgg] @m.xm27.msky130_fd_pr__nfet_01v8[cgs]
+ @m.xm27.msky130_fd_pr__nfet_01v8[cgd] @m.xm27.msky130_fd_pr__nfet_01v8[cgb] @m.xm27.msky130_fd_pr__nfet_01v8[cdg]
+ @m.xm27.msky130_fd_pr__nfet_01v8[cds] @m.xm27.msky130_fd_pr__nfet_01v8[cdd] @m.xm27.msky130_fd_pr__nfet_01v8[cdb]
+ @m.xm27.msky130_fd_pr__nfet_01v8[csg] @m.xm27.msky130_fd_pr__nfet_01v8[css] @m.xm27.msky130_fd_pr__nfet_01v8[csd]
+ @m.xm27.msky130_fd_pr__nfet_01v8[csb] @m.xm27.msky130_fd_pr__nfet_01v8[cbg] @m.xm27.msky130_fd_pr__nfet_01v8[cbs]
+ @m.xm27.msky130_fd_pr__nfet_01v8[cbd] @m.xm27.msky130_fd_pr__nfet_01v8[cbb]

*PFET

save @m.xm91.msky130_fd_pr__pfet_01v8[vds] @m.xm91.msky130_fd_pr__pfet_01v8[gm]
+ @m.xm91.msky130_fd_pr__pfet_01v8[vth] @m.xm91.msky130_fd_pr__pfet_01v8[vgs] @m.xm91.msky130_fd_pr__pfet_01v8[id]
+ @m.xm91.msky130_fd_pr__pfet_01v8[gds] @m.xm91.msky130_fd_pr__pfet_01v8[cgg] @m.xm91.msky130_fd_pr__pfet_01v8[cgs]
+ @m.xm91.msky130_fd_pr__pfet_01v8[cgd] @m.xm91.msky130_fd_pr__pfet_01v8[cgb] @m.xm91.msky130_fd_pr__pfet_01v8[cdg]
+ @m.xm91.msky130_fd_pr__pfet_01v8[cds] @m.xm91.msky130_fd_pr__pfet_01v8[cdd] @m.xm91.msky130_fd_pr__pfet_01v8[cdb]
+ @m.xm91.msky130_fd_pr__pfet_01v8[csg] @m.xm91.msky130_fd_pr__pfet_01v8[css] @m.xm91.msky130_fd_pr__pfet_01v8[csd]
+ @m.xm91.msky130_fd_pr__pfet_01v8[csb] @m.xm91.msky130_fd_pr__pfet_01v8[cbg] @m.xm91.msky130_fd_pr__pfet_01v8[cbs]
+ @m.xm91.msky130_fd_pr__pfet_01v8[cbd] @m.xm91.msky130_fd_pr__pfet_01v8[cbb]
save @m.xm4.msky130_fd_pr__pfet_01v8[vds] @m.xm4.msky130_fd_pr__pfet_01v8[gm]
+ @m.xm4.msky130_fd_pr__pfet_01v8[vth] @m.xm4.msky130_fd_pr__pfet_01v8[vgs] @m.xm4.msky130_fd_pr__pfet_01v8[id]
+ @m.xm4.msky130_fd_pr__pfet_01v8[gds] @m.xm4.msky130_fd_pr__pfet_01v8[cgg] @m.xm4.msky130_fd_pr__pfet_01v8[cgs]
+ @m.xm4.msky130_fd_pr__pfet_01v8[cgd] @m.xm4.msky130_fd_pr__pfet_01v8[cgb] @m.xm4.msky130_fd_pr__pfet_01v8[cdg]
+ @m.xm4.msky130_fd_pr__pfet_01v8[cds] @m.xm4.msky130_fd_pr__pfet_01v8[cdd] @m.xm4.msky130_fd_pr__pfet_01v8[cdb]
+ @m.xm4.msky130_fd_pr__pfet_01v8[csg] @m.xm4.msky130_fd_pr__pfet_01v8[css] @m.xm4.msky130_fd_pr__pfet_01v8[csd]
+ @m.xm4.msky130_fd_pr__pfet_01v8[csb] @m.xm4.msky130_fd_pr__pfet_01v8[cbg] @m.xm4.msky130_fd_pr__pfet_01v8[cbs]
+ @m.xm4.msky130_fd_pr__pfet_01v8[cbd] @m.xm4.msky130_fd_pr__pfet_01v8[cbb]
save @m.xm5.msky130_fd_pr__pfet_01v8[vds] @m.xm5.msky130_fd_pr__pfet_01v8[gm]
+ @m.xm5.msky130_fd_pr__pfet_01v8[vth] @m.xm5.msky130_fd_pr__pfet_01v8[vgs] @m.xm5.msky130_fd_pr__pfet_01v8[id]
+ @m.xm5.msky130_fd_pr__pfet_01v8[gds] @m.xm5.msky130_fd_pr__pfet_01v8[cgg] @m.xm5.msky130_fd_pr__pfet_01v8[cgs]
+ @m.xm5.msky130_fd_pr__pfet_01v8[cgd] @m.xm5.msky130_fd_pr__pfet_01v8[cgb] @m.xm5.msky130_fd_pr__pfet_01v8[cdg]
+ @m.xm5.msky130_fd_pr__pfet_01v8[cds] @m.xm5.msky130_fd_pr__pfet_01v8[cdd] @m.xm5.msky130_fd_pr__pfet_01v8[cdb]
+ @m.xm5.msky130_fd_pr__pfet_01v8[csg] @m.xm5.msky130_fd_pr__pfet_01v8[css] @m.xm5.msky130_fd_pr__pfet_01v8[csd]
+ @m.xm5.msky130_fd_pr__pfet_01v8[csb] @m.xm5.msky130_fd_pr__pfet_01v8[cbg] @m.xm5.msky130_fd_pr__pfet_01v8[cbs]
+ @m.xm5.msky130_fd_pr__pfet_01v8[cbd] @m.xm5.msky130_fd_pr__pfet_01v8[cbb]
save @m.xm9.msky130_fd_pr__pfet_01v8[vds] @m.xm9.msky130_fd_pr__pfet_01v8[gm]
+ @m.xm9.msky130_fd_pr__pfet_01v8[vth] @m.xm9.msky130_fd_pr__pfet_01v8[vgs] @m.xm9.msky130_fd_pr__pfet_01v8[id]
+ @m.xm9.msky130_fd_pr__pfet_01v8[gds] @m.xm9.msky130_fd_pr__pfet_01v8[cgg] @m.xm9.msky130_fd_pr__pfet_01v8[cgs]
+ @m.xm9.msky130_fd_pr__pfet_01v8[cgd] @m.xm9.msky130_fd_pr__pfet_01v8[cgb] @m.xm9.msky130_fd_pr__pfet_01v8[cdg]
+ @m.xm9.msky130_fd_pr__pfet_01v8[cds] @m.xm9.msky130_fd_pr__pfet_01v8[cdd] @m.xm9.msky130_fd_pr__pfet_01v8[cdb]
+ @m.xm9.msky130_fd_pr__pfet_01v8[csg] @m.xm9.msky130_fd_pr__pfet_01v8[css] @m.xm9.msky130_fd_pr__pfet_01v8[csd]
+ @m.xm9.msky130_fd_pr__pfet_01v8[csb] @m.xm9.msky130_fd_pr__pfet_01v8[cbg] @m.xm9.msky130_fd_pr__pfet_01v8[cbs]
+ @m.xm9.msky130_fd_pr__pfet_01v8[cbd] @m.xm9.msky130_fd_pr__pfet_01v8[cbb]
save @m.xm10.msky130_fd_pr__pfet_01v8[vds] @m.xm10.msky130_fd_pr__pfet_01v8[gm]
+ @m.xm10.msky130_fd_pr__pfet_01v8[vth] @m.xm10.msky130_fd_pr__pfet_01v8[vgs] @m.xm10.msky130_fd_pr__pfet_01v8[id]
+ @m.xm10.msky130_fd_pr__pfet_01v8[gds] @m.xm10.msky130_fd_pr__pfet_01v8[cgg] @m.xm10.msky130_fd_pr__pfet_01v8[cgs]
+ @m.xm10.msky130_fd_pr__pfet_01v8[cgd] @m.xm10.msky130_fd_pr__pfet_01v8[cgb] @m.xm10.msky130_fd_pr__pfet_01v8[cdg]
+ @m.xm10.msky130_fd_pr__pfet_01v8[cds] @m.xm10.msky130_fd_pr__pfet_01v8[cdd] @m.xm10.msky130_fd_pr__pfet_01v8[cdb]
+ @m.xm10.msky130_fd_pr__pfet_01v8[csg] @m.xm10.msky130_fd_pr__pfet_01v8[css] @m.xm10.msky130_fd_pr__pfet_01v8[csd]
+ @m.xm10.msky130_fd_pr__pfet_01v8[csb] @m.xm10.msky130_fd_pr__pfet_01v8[cbg] @m.xm10.msky130_fd_pr__pfet_01v8[cbs]
+ @m.xm10.msky130_fd_pr__pfet_01v8[cbd] @m.xm10.msky130_fd_pr__pfet_01v8[cbb]
save @m.xm13.msky130_fd_pr__pfet_01v8[vds] @m.xm13.msky130_fd_pr__pfet_01v8[gm]
+ @m.xm13.msky130_fd_pr__pfet_01v8[vth] @m.xm13.msky130_fd_pr__pfet_01v8[vgs] @m.xm13.msky130_fd_pr__pfet_01v8[id]
+ @m.xm13.msky130_fd_pr__pfet_01v8[gds] @m.xm13.msky130_fd_pr__pfet_01v8[cgg] @m.xm13.msky130_fd_pr__pfet_01v8[cgs]
+ @m.xm13.msky130_fd_pr__pfet_01v8[cgd] @m.xm13.msky130_fd_pr__pfet_01v8[cgb] @m.xm13.msky130_fd_pr__pfet_01v8[cdg]
+ @m.xm13.msky130_fd_pr__pfet_01v8[cds] @m.xm13.msky130_fd_pr__pfet_01v8[cdd] @m.xm13.msky130_fd_pr__pfet_01v8[cdb]
+ @m.xm13.msky130_fd_pr__pfet_01v8[csg] @m.xm13.msky130_fd_pr__pfet_01v8[css] @m.xm13.msky130_fd_pr__pfet_01v8[csd]
+ @m.xm13.msky130_fd_pr__pfet_01v8[csb] @m.xm13.msky130_fd_pr__pfet_01v8[cbg] @m.xm13.msky130_fd_pr__pfet_01v8[cbs]
+ @m.xm13.msky130_fd_pr__pfet_01v8[cbd] @m.xm13.msky130_fd_pr__pfet_01v8[cbb]
save @m.xm14.msky130_fd_pr__pfet_01v8[vds] @m.xm14.msky130_fd_pr__pfet_01v8[gm]
+ @m.xm14.msky130_fd_pr__pfet_01v8[vth] @m.xm14.msky130_fd_pr__pfet_01v8[vgs] @m.xm14.msky130_fd_pr__pfet_01v8[id]
+ @m.xm14.msky130_fd_pr__pfet_01v8[gds] @m.xm14.msky130_fd_pr__pfet_01v8[cgg] @m.xm14.msky130_fd_pr__pfet_01v8[cgs]
+ @m.xm14.msky130_fd_pr__pfet_01v8[cgd] @m.xm14.msky130_fd_pr__pfet_01v8[cgb] @m.xm14.msky130_fd_pr__pfet_01v8[cdg]
+ @m.xm14.msky130_fd_pr__pfet_01v8[cds] @m.xm14.msky130_fd_pr__pfet_01v8[cdd] @m.xm14.msky130_fd_pr__pfet_01v8[cdb]
+ @m.xm14.msky130_fd_pr__pfet_01v8[csg] @m.xm14.msky130_fd_pr__pfet_01v8[css] @m.xm14.msky130_fd_pr__pfet_01v8[csd]
+ @m.xm14.msky130_fd_pr__pfet_01v8[csb] @m.xm14.msky130_fd_pr__pfet_01v8[cbg] @m.xm14.msky130_fd_pr__pfet_01v8[cbs]
+ @m.xm14.msky130_fd_pr__pfet_01v8[cbd] @m.xm14.msky130_fd_pr__pfet_01v8[cbb]
save @m.xm24.msky130_fd_pr__pfet_01v8[vds] @m.xm24.msky130_fd_pr__pfet_01v8[gm]
+ @m.xm24.msky130_fd_pr__pfet_01v8[vth] @m.xm24.msky130_fd_pr__pfet_01v8[vgs] @m.xm24.msky130_fd_pr__pfet_01v8[id]
+ @m.xm24.msky130_fd_pr__pfet_01v8[gds] @m.xm24.msky130_fd_pr__pfet_01v8[cgg] @m.xm24.msky130_fd_pr__pfet_01v8[cgs]
+ @m.xm24.msky130_fd_pr__pfet_01v8[cgd] @m.xm24.msky130_fd_pr__pfet_01v8[cgb] @m.xm24.msky130_fd_pr__pfet_01v8[cdg]
+ @m.xm24.msky130_fd_pr__pfet_01v8[cds] @m.xm24.msky130_fd_pr__pfet_01v8[cdd] @m.xm24.msky130_fd_pr__pfet_01v8[cdb]
+ @m.xm24.msky130_fd_pr__pfet_01v8[csg] @m.xm24.msky130_fd_pr__pfet_01v8[css] @m.xm24.msky130_fd_pr__pfet_01v8[csd]
+ @m.xm24.msky130_fd_pr__pfet_01v8[csb] @m.xm24.msky130_fd_pr__pfet_01v8[cbg] @m.xm24.msky130_fd_pr__pfet_01v8[cbs]
+ @m.xm24.msky130_fd_pr__pfet_01v8[cbd] @m.xm24.msky130_fd_pr__pfet_01v8[cbb]
save @m.xm25.msky130_fd_pr__pfet_01v8[vds] @m.xm25.msky130_fd_pr__pfet_01v8[gm]
+ @m.xm25.msky130_fd_pr__pfet_01v8[vth] @m.xm25.msky130_fd_pr__pfet_01v8[vgs] @m.xm25.msky130_fd_pr__pfet_01v8[id]
+ @m.xm25.msky130_fd_pr__pfet_01v8[gds] @m.xm25.msky130_fd_pr__pfet_01v8[cgg] @m.xm25.msky130_fd_pr__pfet_01v8[cgs]
+ @m.xm25.msky130_fd_pr__pfet_01v8[cgd] @m.xm25.msky130_fd_pr__pfet_01v8[cgb] @m.xm25.msky130_fd_pr__pfet_01v8[cdg]
+ @m.xm25.msky130_fd_pr__pfet_01v8[cds] @m.xm25.msky130_fd_pr__pfet_01v8[cdd] @m.xm25.msky130_fd_pr__pfet_01v8[cdb]
+ @m.xm25.msky130_fd_pr__pfet_01v8[csg] @m.xm25.msky130_fd_pr__pfet_01v8[css] @m.xm25.msky130_fd_pr__pfet_01v8[csd]
+ @m.xm25.msky130_fd_pr__pfet_01v8[csb] @m.xm25.msky130_fd_pr__pfet_01v8[cbg] @m.xm25.msky130_fd_pr__pfet_01v8[cbs]
+ @m.xm25.msky130_fd_pr__pfet_01v8[cbd] @m.xm25.msky130_fd_pr__pfet_01v8[cbb]

op
write flattened.raw
.endc


.control
*tran .001n 10u 5m
*plot Vout_n

*tran 10u 5m
*plot Vcmfb
*plot Vcm1

ac dec 50 1k 10G
plot vdb(Vout_p)
*plot vdb(Vcm1)
*plot vp(Vcm1)*57.296

*exit
.endc


**** end user architecture code
**.ends
.GLOBAL GND
.end
